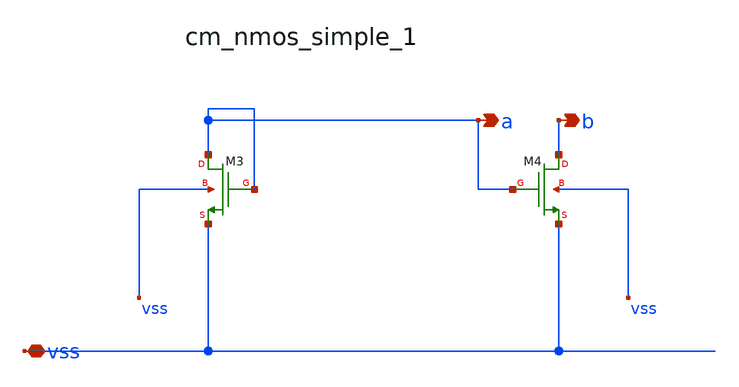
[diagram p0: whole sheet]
** sch_path: analog-db/raw/amp_022_fer_two_stage/hier/blocks/cm_nmos_simple_1.sch
**.subckt cm_nmos_simple_1 vss a b
*.iopin vss
*.opin a
*.opin b
XM3 a a vss vss sg13_lv_nmos w=x_dut_xm3_w l=x_dut_xm3_l ng=1 m=x_dut_xm3_m
XM4 b a vss vss sg13_lv_nmos w=x_dut_xm4_w l=x_dut_xm4_l ng=1 m=x_dut_xm4_m
**.ends
.end
